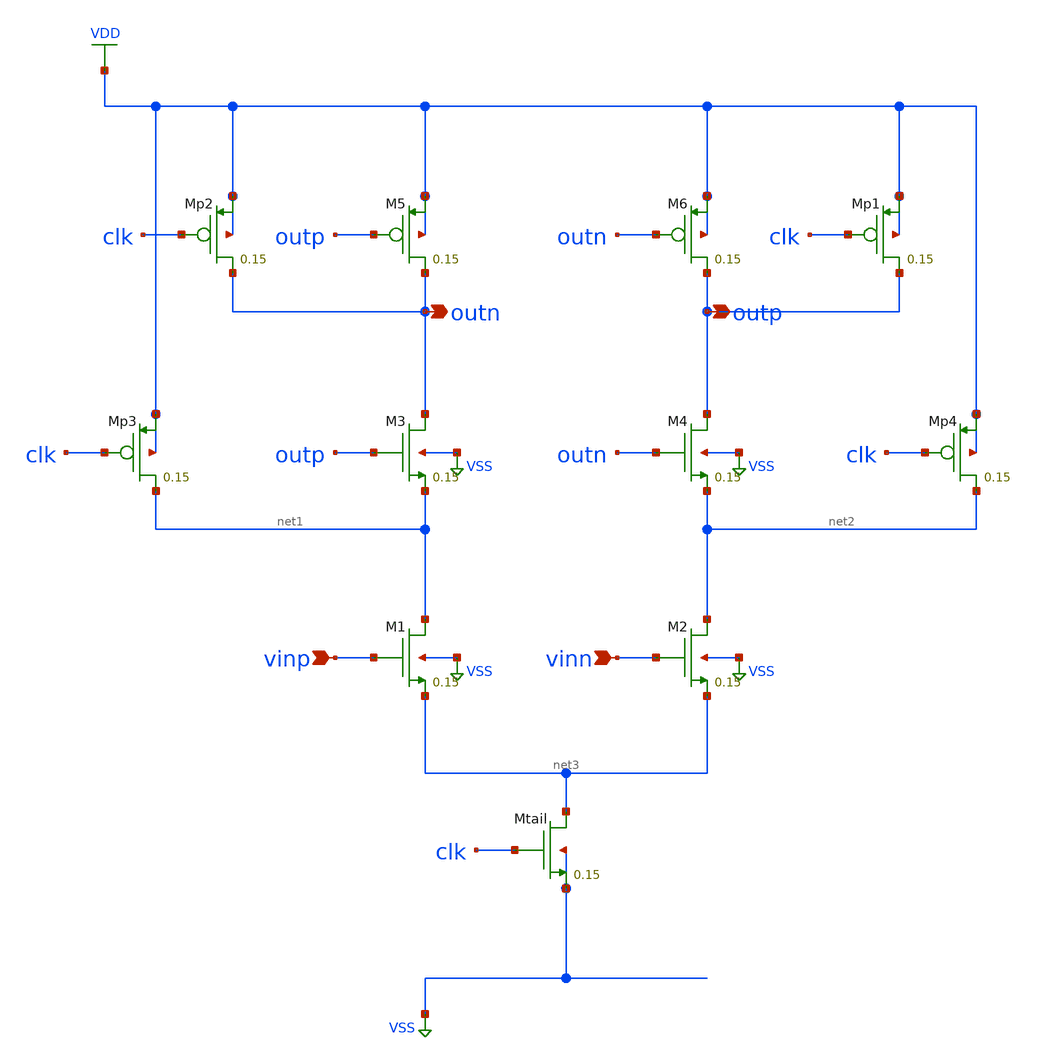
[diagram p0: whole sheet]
** sch_path: eda/hero/schematics/strongarm_sa.sch
**.subckt strongarm_sa vinp vinn outn outp
*.ipin vinp
*.ipin vinn
*.opin outn
*.opin outp
XM5 outn outp VDD VDD sky130_fd_pr__sky130_fd_pr__pfet_01v8 L=0.15 W=2 nrd='0.29 / W' nrs='0.29 / W'
+ sa=0 sb=0 sd=0 mult=1 m=1
XM6 outp outn VDD VDD sky130_fd_pr__sky130_fd_pr__pfet_01v8 L=0.15 W=2 nrd='0.29 / W' nrs='0.29 / W'
+ sa=0 sb=0 sd=0 mult=1 m=1
XMp2 outn clk VDD VDD sky130_fd_pr__sky130_fd_pr__pfet_01v8 L=0.15 W=2 nrd='0.29 / W' nrs='0.29 / W'
+ sa=0 sb=0 sd=0 mult=1 m=1
XMp1 outp clk VDD VDD sky130_fd_pr__sky130_fd_pr__pfet_01v8 L=0.15 W=2 nrd='0.29 / W' nrs='0.29 / W'
+ sa=0 sb=0 sd=0 mult=1 m=1
XM3 outn outp net1 VSS sky130_fd_pr__sky130_fd_pr__nfet_01v8 L=0.15 W=2 nrd='0.29 / W' nrs='0.29 / W'
+ sa=0 sb=0 sd=0 mult=1 m=1
XM4 outp outn net2 VSS sky130_fd_pr__sky130_fd_pr__nfet_01v8 L=0.15 W=2 nrd='0.29 / W' nrs='0.29 / W'
+ sa=0 sb=0 sd=0 mult=1 m=1
XMp3 net1 clk VDD VDD sky130_fd_pr__sky130_fd_pr__pfet_01v8 L=0.15 W=2 nrd='0.29 / W' nrs='0.29 / W'
+ sa=0 sb=0 sd=0 mult=1 m=1
XMp4 net2 clk VDD VDD sky130_fd_pr__sky130_fd_pr__pfet_01v8 L=0.15 W=2 nrd='0.29 / W' nrs='0.29 / W'
+ sa=0 sb=0 sd=0 mult=1 m=1
XM1 net1 vinp net3 VSS sky130_fd_pr__sky130_fd_pr__nfet_01v8 L=0.15 W=4 nrd='0.29 / W' nrs='0.29 / W'
+ sa=0 sb=0 sd=0 mult=1 m=1
XM2 net2 vinn net3 VSS sky130_fd_pr__sky130_fd_pr__nfet_01v8 L=0.15 W=4 nrd='0.29 / W' nrs='0.29 / W'
+ sa=0 sb=0 sd=0 mult=1 m=1
XMtail net3 clk VSS VSS sky130_fd_pr__sky130_fd_pr__nfet_01v8 L=0.15 W=4 nrd='0.29 / W' nrs='0.29 / W'
+ sa=0 sb=0 sd=0 mult=1 m=1
**.ends
.GLOBAL VSS
.GLOBAL VDD
.end
